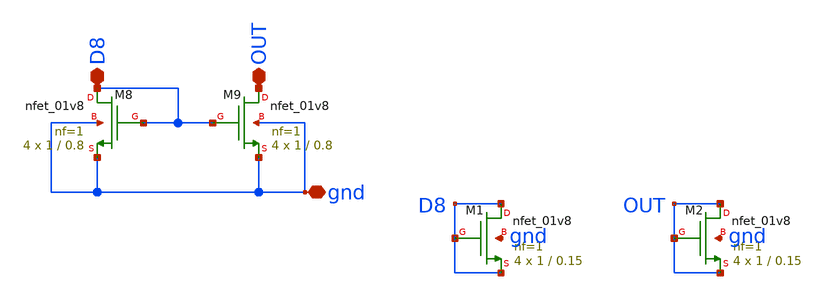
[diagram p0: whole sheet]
** sch_path: OP_Amp/mag/nmosamp.sch
**.subckt nmosamp gnd D8 OUT
*.iopin gnd
*.iopin D8
*.iopin OUT
XM8 D8 D8 gnd gnd sky130_fd_pr__nfet_01v8 L=0.8 W=1 nf=1 ad='int((nf+1)/2) * W/nf * 0.29' as='int((nf+2)/2) * W/nf * 0.29'
+ pd='2*int((nf+1)/2) * (W/nf + 0.29)' ps='2*int((nf+2)/2) * (W/nf + 0.29)' nrd='0.29 / W' nrs='0.29 / W'
+ sa=0 sb=0 sd=0 mult=4 m=4
XM9 OUT D8 gnd gnd sky130_fd_pr__nfet_01v8 L=0.8 W=1 nf=1 ad='int((nf+1)/2) * W/nf * 0.29' as='int((nf+2)/2) * W/nf * 0.29'
+ pd='2*int((nf+1)/2) * (W/nf + 0.29)' ps='2*int((nf+2)/2) * (W/nf + 0.29)' nrd='0.29 / W' nrs='0.29 / W'
+ sa=0 sb=0 sd=0 mult=4 m=4
XM1 D8 D8 D8 gnd sky130_fd_pr__nfet_01v8 L=0.15 W=1 nf=1 ad='int((nf+1)/2) * W/nf * 0.29' as='int((nf+2)/2) * W/nf * 0.29'
+ pd='2*int((nf+1)/2) * (W/nf + 0.29)' ps='2*int((nf+2)/2) * (W/nf + 0.29)' nrd='0.29 / W' nrs='0.29 / W'
+ sa=0 sb=0 sd=0 mult=4 m=4
XM2 OUT OUT OUT gnd sky130_fd_pr__nfet_01v8 L=0.15 W=1 nf=1 ad='int((nf+1)/2) * W/nf * 0.29' as='int((nf+2)/2) * W/nf * 0.29'
+ pd='2*int((nf+1)/2) * (W/nf + 0.29)' ps='2*int((nf+2)/2) * (W/nf + 0.29)' nrd='0.29 / W' nrs='0.29 / W'
+ sa=0 sb=0 sd=0 mult=4 m=4
**.ends
.end
